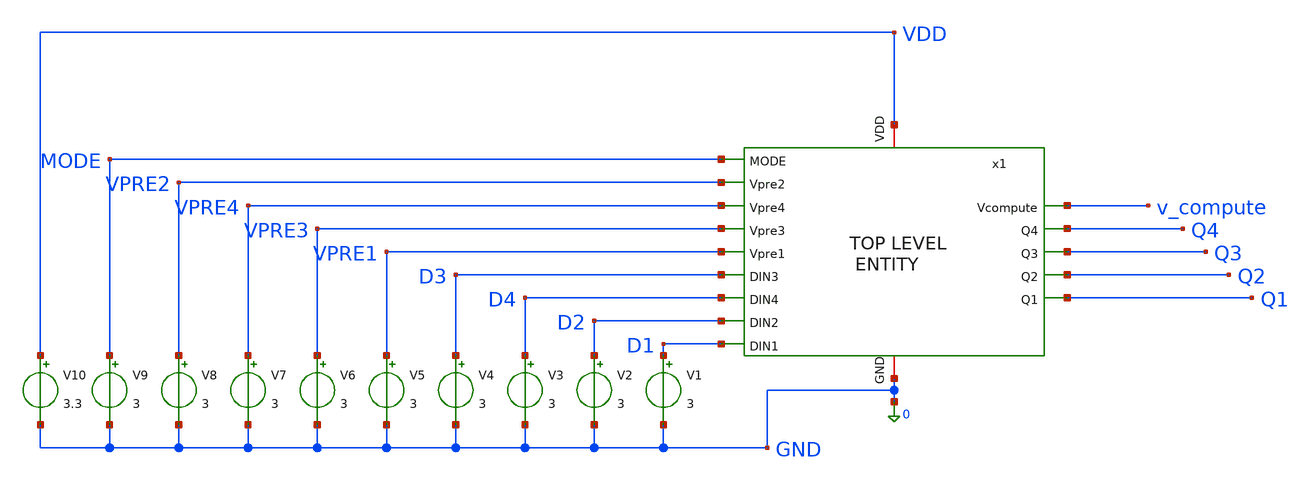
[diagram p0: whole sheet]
** sch_path: src/schematic/INTEGRASI/integrasi_TB.sch
**.subckt integrasi_TB
x1 VDD MODE 0 VPRE2 VPRE4 VPRE3 VPRE1 D3 D4 v_compute Q4 Q3 Q2 Q1 D2 D1 integrasi
V1 D1 0 3
V2 D2 0 3
V3 D4 0 3
V4 D3 0 3
V5 VPRE1 0 3
V6 VPRE3 0 3
V7 VPRE4 0 3
V8 VPRE2 0 3
V9 MODE 0 3
V10 VDD 0 3.3
**.ends

* expanding   symbol:  src/schematic/INTEGRASI/integrasi.sym # of pins=16
** sym_path: src/schematic/INTEGRASI/integrasi.sym
** sch_path: src/schematic/INTEGRASI/integrasi.sch
.subckt integrasi VDD MODE GND Vpre2 Vpre4 Vpre3 Vpre1 DIN3 DIN4 Vcompute Q4 Q3 Q2 Q1 DIN2 DIN1
*.ipin Vpre1
*.ipin Vpre2
*.ipin Vpre3
*.ipin Vpre4
*.ipin DIN4
*.ipin DIN3
*.ipin DIN2
*.ipin DIN1
*.ipin MODE
*.iopin VDD
*.iopin GND
*.opin Vcompute
*.opin Q4
*.opin Q3
*.opin Q2
*.opin Q1
x1 net1 net2 net4 net3 net19 net20 net21 net18 net5 net7 net27 net26 net28 net29 Q4 Q3 Q2 Q1 net8
+ net12 Vcompute memori
x2 net5 net2 Vpre2 net6 MODE transgate
x3 net5 net3 Vpre3 net6 MODE transgate
x4 net5 net4 Vpre4 net6 MODE transgate
x5 net5 net1 Vpre1 net6 MODE transgate
x6 VDD net7 net11 net8 net10 transgate
x7 VDD net7 VDD net8 net9 transgate
x8 VDD net10 net9 net8 inverter
x9 VDD net11 net8 net13 net14 net15 net16 dac
x10 net5 net1 net12 net2 net3 net4 net8 en_compute
x11 VDD net15 DIN2 net8 MODE transgate
x12 VDD net14 DIN4 net8 MODE transgate
x13 VDD net13 DIN3 net8 MODE transgate
x14 VDD net16 DIN1 net8 MODE transgate
x15 VDD net20 DIN2 GND net17 transgate
x16 VDD net19 DIN4 GND net17 transgate
x17 VDD net18 DIN3 GND net17 transgate
x18 VDD net21 DIN1 GND net17 transgate
x19 VDD net23 net20 GND net17 transgate
x20 VDD net24 net19 GND net17 transgate
x21 VDD net25 net18 GND net17 transgate
x22 VDD net22 net21 GND net17 transgate
x23 VDD net25 net29 GND inverter
x24 VDD net24 net28 GND inverter
x25 VDD net23 net26 GND inverter
x26 VDD net22 net27 GND inverter
x27 VDD MODE net17 GND inverter
.ends


* expanding   symbol:  memori.sym # of pins=21
** sym_path: src/schematic/MEMORY/memori.sym
** sch_path: src/schematic/MEMORY/memori.sch
.subckt memori Vpre1 Vpre2 Vpre4 Vpre3 BL4 BL2 BL1 BL3 VDD WL BLB1 BLB2 BLB4 BLB3 Q4 Q3 Q2 Q1 GND
+ en_comp Vout
*.iopin GND
*.iopin VDD
*.iopin WL
*.iopin Q1
*.iopin Q2
*.iopin Q3
*.iopin Q4
*.iopin Vpre4
*.iopin Vpre3
*.iopin Vpre2
*.iopin Vpre1
*.iopin en_comp
*.iopin Vout
*.iopin BLB1
*.iopin BLB2
*.iopin BLB3
*.iopin BLB4
*.iopin BL1
*.iopin BL2
*.iopin BL3
*.iopin BL4
x1 net1 net2 net3 net4 net5 net6 6T4bit
x2 net7 net8 net9 net10 net11 GND 6T4bit
x3 net12 net13 net14 net15 net16 GND 6T4bit
x4 net17 net18 net19 net20 net21 net22 6T4bit
XM1 GND en_comp BLB4 VDD pfet_03v3 L=0.28u W=0.22u nf=1 ad='int((nf+1)/2) * W/nf * 0.18u' as='int((nf+2)/2) * W/nf * 0.18u'
+ pd='2*int((nf+1)/2) * (W/nf + 0.18u)' ps='2*int((nf+2)/2) * (W/nf + 0.18u)' nrd='0.18u / W' nrs='0.18u / W'
+ sa=0 sb=0 sd=0 m=1
XM2 GND en_comp BLB3 VDD pfet_03v3 L=0.28u W=0.22u nf=1 ad='int((nf+1)/2) * W/nf * 0.18u' as='int((nf+2)/2) * W/nf * 0.18u'
+ pd='2*int((nf+1)/2) * (W/nf + 0.18u)' ps='2*int((nf+2)/2) * (W/nf + 0.18u)' nrd='0.18u / W' nrs='0.18u / W'
+ sa=0 sb=0 sd=0 m=1
XM3 GND en_comp BLB2 VDD pfet_03v3 L=0.28u W=0.22u nf=1 ad='int((nf+1)/2) * W/nf * 0.18u' as='int((nf+2)/2) * W/nf * 0.18u'
+ pd='2*int((nf+1)/2) * (W/nf + 0.18u)' ps='2*int((nf+2)/2) * (W/nf + 0.18u)' nrd='0.18u / W' nrs='0.18u / W'
+ sa=0 sb=0 sd=0 m=1
XM4 GND en_comp BLB1 VDD pfet_03v3 L=0.28u W=0.22u nf=1 ad='int((nf+1)/2) * W/nf * 0.18u' as='int((nf+2)/2) * W/nf * 0.18u'
+ pd='2*int((nf+1)/2) * (W/nf + 0.18u)' ps='2*int((nf+2)/2) * (W/nf + 0.18u)' nrd='0.18u / W' nrs='0.18u / W'
+ sa=0 sb=0 sd=0 m=1
XM5 BLB4 en_comp GND GND nfet_03v3 L=0.28u W=0.22u nf=1 ad='int((nf+1)/2) * W/nf * 0.18u' as='int((nf+2)/2) * W/nf * 0.18u'
+ pd='2*int((nf+1)/2) * (W/nf + 0.18u)' ps='2*int((nf+2)/2) * (W/nf + 0.18u)' nrd='0.18u / W' nrs='0.18u / W'
+ sa=0 sb=0 sd=0 m=1
XM6 BLB3 en_comp GND GND nfet_03v3 L=0.28u W=0.22u nf=1 ad='int((nf+1)/2) * W/nf * 0.18u' as='int((nf+2)/2) * W/nf * 0.18u'
+ pd='2*int((nf+1)/2) * (W/nf + 0.18u)' ps='2*int((nf+2)/2) * (W/nf + 0.18u)' nrd='0.18u / W' nrs='0.18u / W'
+ sa=0 sb=0 sd=0 m=1
XM7 BLB2 en_comp GND GND nfet_03v3 L=0.28u W=0.22u nf=1 ad='int((nf+1)/2) * W/nf * 0.18u' as='int((nf+2)/2) * W/nf * 0.18u'
+ pd='2*int((nf+1)/2) * (W/nf + 0.18u)' ps='2*int((nf+2)/2) * (W/nf + 0.18u)' nrd='0.18u / W' nrs='0.18u / W'
+ sa=0 sb=0 sd=0 m=1
XM8 BLB1 en_comp GND GND nfet_03v3 L=0.28u W=0.22u nf=1 ad='int((nf+1)/2) * W/nf * 0.18u' as='int((nf+2)/2) * W/nf * 0.18u'
+ pd='2*int((nf+1)/2) * (W/nf + 0.18u)' ps='2*int((nf+2)/2) * (W/nf + 0.18u)' nrd='0.18u / W' nrs='0.18u / W'
+ sa=0 sb=0 sd=0 m=1
XM9 BLB4 Vpre4 VDD VDD pfet_03v3 L=0.28u W=0.22u nf=1 ad='int((nf+1)/2) * W/nf * 0.18u' as='int((nf+2)/2) * W/nf * 0.18u'
+ pd='2*int((nf+1)/2) * (W/nf + 0.18u)' ps='2*int((nf+2)/2) * (W/nf + 0.18u)' nrd='0.18u / W' nrs='0.18u / W'
+ sa=0 sb=0 sd=0 m=1
XM10 BLB3 Vpre3 VDD VDD pfet_03v3 L=0.28u W=0.22u nf=1 ad='int((nf+1)/2) * W/nf * 0.18u' as='int((nf+2)/2) * W/nf * 0.18u'
+ pd='2*int((nf+1)/2) * (W/nf + 0.18u)' ps='2*int((nf+2)/2) * (W/nf + 0.18u)' nrd='0.18u / W' nrs='0.18u / W'
+ sa=0 sb=0 sd=0 m=1
XM11 BLB2 Vpre2 VDD VDD pfet_03v3 L=0.28u W=0.22u nf=1 ad='int((nf+1)/2) * W/nf * 0.18u' as='int((nf+2)/2) * W/nf * 0.18u'
+ pd='2*int((nf+1)/2) * (W/nf + 0.18u)' ps='2*int((nf+2)/2) * (W/nf + 0.18u)' nrd='0.18u / W' nrs='0.18u / W'
+ sa=0 sb=0 sd=0 m=1
XM12 BLB1 Vpre1 VDD VDD pfet_03v3 L=0.28u W=0.22u nf=1 ad='int((nf+1)/2) * W/nf * 0.18u' as='int((nf+2)/2) * W/nf * 0.18u'
+ pd='2*int((nf+1)/2) * (W/nf + 0.18u)' ps='2*int((nf+2)/2) * (W/nf + 0.18u)' nrd='0.18u / W' nrs='0.18u / W'
+ sa=0 sb=0 sd=0 m=1
XM13 BL1 Vpre1 VDD VDD pfet_03v3 L=0.28u W=0.22u nf=1 ad='int((nf+1)/2) * W/nf * 0.18u' as='int((nf+2)/2) * W/nf * 0.18u'
+ pd='2*int((nf+1)/2) * (W/nf + 0.18u)' ps='2*int((nf+2)/2) * (W/nf + 0.18u)' nrd='0.18u / W' nrs='0.18u / W'
+ sa=0 sb=0 sd=0 m=1
XM14 BL2 Vpre2 VDD VDD pfet_03v3 L=0.28u W=0.22u nf=1 ad='int((nf+1)/2) * W/nf * 0.18u' as='int((nf+2)/2) * W/nf * 0.18u'
+ pd='2*int((nf+1)/2) * (W/nf + 0.18u)' ps='2*int((nf+2)/2) * (W/nf + 0.18u)' nrd='0.18u / W' nrs='0.18u / W'
+ sa=0 sb=0 sd=0 m=1
XM15 BL3 Vpre3 VDD VDD pfet_03v3 L=0.28u W=0.22u nf=1 ad='int((nf+1)/2) * W/nf * 0.18u' as='int((nf+2)/2) * W/nf * 0.18u'
+ pd='2*int((nf+1)/2) * (W/nf + 0.18u)' ps='2*int((nf+2)/2) * (W/nf + 0.18u)' nrd='0.18u / W' nrs='0.18u / W'
+ sa=0 sb=0 sd=0 m=1
XM16 BL4 Vpre4 VDD VDD pfet_03v3 L=0.28u W=0.22u nf=1 ad='int((nf+1)/2) * W/nf * 0.18u' as='int((nf+2)/2) * W/nf * 0.18u'
+ pd='2*int((nf+1)/2) * (W/nf + 0.18u)' ps='2*int((nf+2)/2) * (W/nf + 0.18u)' nrd='0.18u / W' nrs='0.18u / W'
+ sa=0 sb=0 sd=0 m=1
XM17 BLB4 Vpre4 BL4 net23 pfet_03v3 L=0.28u W=0.22u nf=1 ad='int((nf+1)/2) * W/nf * 0.18u' as='int((nf+2)/2) * W/nf * 0.18u'
+ pd='2*int((nf+1)/2) * (W/nf + 0.18u)' ps='2*int((nf+2)/2) * (W/nf + 0.18u)' nrd='0.18u / W' nrs='0.18u / W'
+ sa=0 sb=0 sd=0 m=1
XM18 BLB3 Vpre3 BL3 net24 pfet_03v3 L=0.28u W=0.22u nf=1 ad='int((nf+1)/2) * W/nf * 0.18u' as='int((nf+2)/2) * W/nf * 0.18u'
+ pd='2*int((nf+1)/2) * (W/nf + 0.18u)' ps='2*int((nf+2)/2) * (W/nf + 0.18u)' nrd='0.18u / W' nrs='0.18u / W'
+ sa=0 sb=0 sd=0 m=1
XM19 BLB2 Vpre2 BL2 net25 pfet_03v3 L=0.28u W=0.22u nf=1 ad='int((nf+1)/2) * W/nf * 0.18u' as='int((nf+2)/2) * W/nf * 0.18u'
+ pd='2*int((nf+1)/2) * (W/nf + 0.18u)' ps='2*int((nf+2)/2) * (W/nf + 0.18u)' nrd='0.18u / W' nrs='0.18u / W'
+ sa=0 sb=0 sd=0 m=1
XM20 BLB1 Vpre1 BL1 net26 pfet_03v3 L=0.28u W=0.22u nf=1 ad='int((nf+1)/2) * W/nf * 0.18u' as='int((nf+2)/2) * W/nf * 0.18u'
+ pd='2*int((nf+1)/2) * (W/nf + 0.18u)' ps='2*int((nf+2)/2) * (W/nf + 0.18u)' nrd='0.18u / W' nrs='0.18u / W'
+ sa=0 sb=0 sd=0 m=1
.ends


* expanding   symbol:  transgate.sym # of pins=5
** sym_path: src/schematic/INTEGRASI/transgate.sym
** sch_path: src/schematic/INTEGRASI/transgate.sch
.subckt transgate vdd s d gnd c
*.iopin gnd
*.iopin vdd
*.iopin c
*.ipin d
*.opin s
XM1 d c s gnd nfet_03v3 L=0.28u W=0.22u nf=1 ad='int((nf+1)/2) * W/nf * 0.18u' as='int((nf+2)/2) * W/nf * 0.18u'
+ pd='2*int((nf+1)/2) * (W/nf + 0.18u)' ps='2*int((nf+2)/2) * (W/nf + 0.18u)' nrd='0.18u / W' nrs='0.18u / W'
+ sa=0 sb=0 sd=0 m=1
XM2 d net1 s vdd pfet_03v3 L=0.28u W=0.22u nf=1 ad='int((nf+1)/2) * W/nf * 0.18u' as='int((nf+2)/2) * W/nf * 0.18u'
+ pd='2*int((nf+1)/2) * (W/nf + 0.18u)' ps='2*int((nf+2)/2) * (W/nf + 0.18u)' nrd='0.18u / W' nrs='0.18u / W'
+ sa=0 sb=0 sd=0 m=1
x1 vdd c net1 gnd inverter
.ends


* expanding   symbol:  inverter.sym # of pins=4
** sym_path: src/schematic/INTEGRASI/inverter.sym
** sch_path: src/schematic/INTEGRASI/inverter.sch
.subckt inverter vdd vi vo gnd
*.ipin vi
*.opin vo
*.iopin vdd
*.iopin gnd
XM1 vo vi vdd vdd pfet_03v3 L=0.28u W=0.22u nf=1 ad='int((nf+1)/2) * W/nf * 0.18u' as='int((nf+2)/2) * W/nf * 0.18u'
+ pd='2*int((nf+1)/2) * (W/nf + 0.18u)' ps='2*int((nf+2)/2) * (W/nf + 0.18u)' nrd='0.18u / W' nrs='0.18u / W'
+ sa=0 sb=0 sd=0 m=1
XM2 vo vi gnd gnd nfet_03v3 L=0.28u W=0.22u nf=1 ad='int((nf+1)/2) * W/nf * 0.18u' as='int((nf+2)/2) * W/nf * 0.18u'
+ pd='2*int((nf+1)/2) * (W/nf + 0.18u)' ps='2*int((nf+2)/2) * (W/nf + 0.18u)' nrd='0.18u / W' nrs='0.18u / W'
+ sa=0 sb=0 sd=0 m=1
.ends


* expanding   symbol:  dac.sym # of pins=7
** sym_path: src/schematic/INTEGRASI/dac.sym
** sch_path: src/schematic/INTEGRASI/dac.sch
.subckt dac VDD Vout GND V3 V4 V2 V1
*.ipin V1
*.ipin V2
*.ipin V3
*.ipin V4
*.opin Vout
*.iopin VDD
*.iopin GND
R1 VDD Vout 1k m=1
R2 VDD net3 1k m=1
XQ1 net1 net3 V4 V4 nfet_03v3 L=0.28u W=1u nf=1 ad='int((nf+1)/2) * W/nf * 0.18u' as='int((nf+2)/2) * W/nf * 0.18u'
+ pd='2*int((nf+1)/2) * (W/nf + 0.18u)' ps='2*int((nf+2)/2) * (W/nf + 0.18u)' nrd='0.18u / W' nrs='0.18u / W'
+ sa=0 sb=0 sd=0 m=1
XQ2 net4 net3 V4 V4 nfet_03v3 L=0.28u W=2u nf=1 ad='int((nf+1)/2) * W/nf * 0.18u' as='int((nf+2)/2) * W/nf * 0.18u'
+ pd='2*int((nf+1)/2) * (W/nf + 0.18u)' ps='2*int((nf+2)/2) * (W/nf + 0.18u)' nrd='0.18u / W' nrs='0.18u / W'
+ sa=0 sb=0 sd=0 m=1
XQ3 net5 net3 V4 V4 nfet_03v3 L=0.28u W=4u nf=1 ad='int((nf+1)/2) * W/nf * 0.18u' as='int((nf+2)/2) * W/nf * 0.18u'
+ pd='2*int((nf+1)/2) * (W/nf + 0.18u)' ps='2*int((nf+2)/2) * (W/nf + 0.18u)' nrd='0.18u / W' nrs='0.18u / W'
+ sa=0 sb=0 sd=0 m=1
XQ4 net2 net3 V4 V4 nfet_03v3 L=0.28u W=8u nf=1 ad='int((nf+1)/2) * W/nf * 0.18u' as='int((nf+2)/2) * W/nf * 0.18u'
+ pd='2*int((nf+1)/2) * (W/nf + 0.18u)' ps='2*int((nf+2)/2) * (W/nf + 0.18u)' nrd='0.18u / W' nrs='0.18u / W'
+ sa=0 sb=0 sd=0 m=1
XQ0 V4 net3 net3 V4 nfet_03v3 L=0.28u W=1u nf=1 ad='int((nf+1)/2) * W/nf * 0.18u' as='int((nf+2)/2) * W/nf * 0.18u'
+ pd='2*int((nf+1)/2) * (W/nf + 0.18u)' ps='2*int((nf+2)/2) * (W/nf + 0.18u)' nrd='0.18u / W' nrs='0.18u / W'
+ sa=0 sb=0 sd=0 m=1
XTGN1 Vout V1 net1 V4 nfet_03v3 L=0.28u W=5u nf=1 ad='int((nf+1)/2) * W/nf * 0.18u' as='int((nf+2)/2) * W/nf * 0.18u'
+ pd='2*int((nf+1)/2) * (W/nf + 0.18u)' ps='2*int((nf+2)/2) * (W/nf + 0.18u)' nrd='0.18u / W' nrs='0.18u / W'
+ sa=0 sb=0 sd=0 m=1
XTGN2 Vout V2 net4 V4 nfet_03v3 L=0.28u W=5u nf=1 ad='int((nf+1)/2) * W/nf * 0.18u' as='int((nf+2)/2) * W/nf * 0.18u'
+ pd='2*int((nf+1)/2) * (W/nf + 0.18u)' ps='2*int((nf+2)/2) * (W/nf + 0.18u)' nrd='0.18u / W' nrs='0.18u / W'
+ sa=0 sb=0 sd=0 m=1
XTGN3 Vout V3 net5 V4 nfet_03v3 L=0.28u W=5u nf=1 ad='int((nf+1)/2) * W/nf * 0.18u' as='int((nf+2)/2) * W/nf * 0.18u'
+ pd='2*int((nf+1)/2) * (W/nf + 0.18u)' ps='2*int((nf+2)/2) * (W/nf + 0.18u)' nrd='0.18u / W' nrs='0.18u / W'
+ sa=0 sb=0 sd=0 m=1
XTGN4 Vout V4 net2 V4 nfet_03v3 L=0.28u W=5u nf=1 ad='int((nf+1)/2) * W/nf * 0.18u' as='int((nf+2)/2) * W/nf * 0.18u'
+ pd='2*int((nf+1)/2) * (W/nf + 0.18u)' ps='2*int((nf+2)/2) * (W/nf + 0.18u)' nrd='0.18u / W' nrs='0.18u / W'
+ sa=0 sb=0 sd=0 m=1
XTGP1 net1 VB1 Vout VDD pfet_03v3 L=0.28u W=10u nf=1 ad='int((nf+1)/2) * W/nf * 0.18u' as='int((nf+2)/2) * W/nf * 0.18u'
+ pd='2*int((nf+1)/2) * (W/nf + 0.18u)' ps='2*int((nf+2)/2) * (W/nf + 0.18u)' nrd='0.18u / W' nrs='0.18u / W'
+ sa=0 sb=0 sd=0 m=1
XIN1 VB1 V1 V4 V4 nfet_03v3 L=0.28u W=1u nf=1 ad='int((nf+1)/2) * W/nf * 0.18u' as='int((nf+2)/2) * W/nf * 0.18u'
+ pd='2*int((nf+1)/2) * (W/nf + 0.18u)' ps='2*int((nf+2)/2) * (W/nf + 0.18u)' nrd='0.18u / W' nrs='0.18u / W'
+ sa=0 sb=0 sd=0 m=1
XIP1 VB1 V1 VDD VDD pfet_03v3 L=0.28u W=2u nf=1 ad='int((nf+1)/2) * W/nf * 0.18u' as='int((nf+2)/2) * W/nf * 0.18u'
+ pd='2*int((nf+1)/2) * (W/nf + 0.18u)' ps='2*int((nf+2)/2) * (W/nf + 0.18u)' nrd='0.18u / W' nrs='0.18u / W'
+ sa=0 sb=0 sd=0 m=1
XIN2 VB2 V2 V4 V4 nfet_03v3 L=0.28u W=1u nf=1 ad='int((nf+1)/2) * W/nf * 0.18u' as='int((nf+2)/2) * W/nf * 0.18u'
+ pd='2*int((nf+1)/2) * (W/nf + 0.18u)' ps='2*int((nf+2)/2) * (W/nf + 0.18u)' nrd='0.18u / W' nrs='0.18u / W'
+ sa=0 sb=0 sd=0 m=1
XIP2 VB2 V2 VDD VDD pfet_03v3 L=0.28u W=2u nf=1 ad='int((nf+1)/2) * W/nf * 0.18u' as='int((nf+2)/2) * W/nf * 0.18u'
+ pd='2*int((nf+1)/2) * (W/nf + 0.18u)' ps='2*int((nf+2)/2) * (W/nf + 0.18u)' nrd='0.18u / W' nrs='0.18u / W'
+ sa=0 sb=0 sd=0 m=1
XIN3 VB3 V3 V4 V4 nfet_03v3 L=0.28u W=1u nf=1 ad='int((nf+1)/2) * W/nf * 0.18u' as='int((nf+2)/2) * W/nf * 0.18u'
+ pd='2*int((nf+1)/2) * (W/nf + 0.18u)' ps='2*int((nf+2)/2) * (W/nf + 0.18u)' nrd='0.18u / W' nrs='0.18u / W'
+ sa=0 sb=0 sd=0 m=1
XIP3 VB3 V3 VDD VDD pfet_03v3 L=0.28u W=2u nf=1 ad='int((nf+1)/2) * W/nf * 0.18u' as='int((nf+2)/2) * W/nf * 0.18u'
+ pd='2*int((nf+1)/2) * (W/nf + 0.18u)' ps='2*int((nf+2)/2) * (W/nf + 0.18u)' nrd='0.18u / W' nrs='0.18u / W'
+ sa=0 sb=0 sd=0 m=1
XIN4 VB4 V4 V4 V4 nfet_03v3 L=0.28u W=1u nf=1 ad='int((nf+1)/2) * W/nf * 0.18u' as='int((nf+2)/2) * W/nf * 0.18u'
+ pd='2*int((nf+1)/2) * (W/nf + 0.18u)' ps='2*int((nf+2)/2) * (W/nf + 0.18u)' nrd='0.18u / W' nrs='0.18u / W'
+ sa=0 sb=0 sd=0 m=1
XIP4 VB4 V4 VDD VDD pfet_03v3 L=0.28u W=2u nf=1 ad='int((nf+1)/2) * W/nf * 0.18u' as='int((nf+2)/2) * W/nf * 0.18u'
+ pd='2*int((nf+1)/2) * (W/nf + 0.18u)' ps='2*int((nf+2)/2) * (W/nf + 0.18u)' nrd='0.18u / W' nrs='0.18u / W'
+ sa=0 sb=0 sd=0 m=1
XTGP2 net4 VB2 Vout VDD pfet_03v3 L=0.28u W=10u nf=1 ad='int((nf+1)/2) * W/nf * 0.18u' as='int((nf+2)/2) * W/nf * 0.18u'
+ pd='2*int((nf+1)/2) * (W/nf + 0.18u)' ps='2*int((nf+2)/2) * (W/nf + 0.18u)' nrd='0.18u / W' nrs='0.18u / W'
+ sa=0 sb=0 sd=0 m=1
XTGP3 net5 VB3 Vout VDD pfet_03v3 L=0.28u W=10u nf=1 ad='int((nf+1)/2) * W/nf * 0.18u' as='int((nf+2)/2) * W/nf * 0.18u'
+ pd='2*int((nf+1)/2) * (W/nf + 0.18u)' ps='2*int((nf+2)/2) * (W/nf + 0.18u)' nrd='0.18u / W' nrs='0.18u / W'
+ sa=0 sb=0 sd=0 m=1
XTGP4 net2 VB4 Vout VDD pfet_03v3 L=0.28u W=10u nf=1 ad='int((nf+1)/2) * W/nf * 0.18u' as='int((nf+2)/2) * W/nf * 0.18u'
+ pd='2*int((nf+1)/2) * (W/nf + 0.18u)' ps='2*int((nf+2)/2) * (W/nf + 0.18u)' nrd='0.18u / W' nrs='0.18u / W'
+ sa=0 sb=0 sd=0 m=1
.ends


* expanding   symbol:  en_compute.sym # of pins=7
** sym_path: src/schematic/EN-COMPUTE/en_compute.sym
** sch_path: src/schematic/EN-COMPUTE/en_compute.sch
.subckt en_compute VDD A en_cmpt B C D GND
*.iopin VDD
*.iopin GND
*.iopin en_cmpt
*.iopin D
*.iopin C
*.iopin B
*.iopin A
x1 VDD A B net1 GND norGate
x3 VDD net1 C net2 GND norGate
x5 VDD net2 D en_cmpt GND norGate
.ends


* expanding   symbol:  src/schematic/6T4BIT/6T4bit.sch # of pins=6
** sym_path: src/schematic/6T4BIT/6T4bit.sch
** sch_path: src/schematic/6T4BIT/6T4bit.sch
.subckt 6T4bit VDD WL BLB BL Q GND
*.iopin BLB
*.iopin GND
*.iopin Q
*.iopin VDD
*.iopin BL
*.iopin WL
XSR1_M6 Q WL BL GND nfet_03v3 L=0.28u W=0.22u nf=1 ad='int((nf+1)/2) * W/nf * 0.18u' as='int((nf+2)/2) * W/nf * 0.18u'
+ pd='2*int((nf+1)/2) * (W/nf + 0.18u)' ps='2*int((nf+2)/2) * (W/nf + 0.18u)' nrd='0.18u / W' nrs='0.18u / W'
+ sa=0 sb=0 sd=0 m=1
XSR1_M3 VDD net1 Q VDD pfet_03v3 L=0.28u W=0.22u nf=1 ad='int((nf+1)/2) * W/nf * 0.18u' as='int((nf+2)/2) * W/nf * 0.18u'
+ pd='2*int((nf+1)/2) * (W/nf + 0.18u)' ps='2*int((nf+2)/2) * (W/nf + 0.18u)' nrd='0.18u / W' nrs='0.18u / W'
+ sa=0 sb=0 sd=0 m=1
XSR1_M4 net1 net2 VDD VDD pfet_03v3 L=0.28u W=0.22u nf=1 ad='int((nf+1)/2) * W/nf * 0.18u' as='int((nf+2)/2) * W/nf * 0.18u'
+ pd='2*int((nf+1)/2) * (W/nf + 0.18u)' ps='2*int((nf+2)/2) * (W/nf + 0.18u)' nrd='0.18u / W' nrs='0.18u / W'
+ sa=0 sb=0 sd=0 m=1
XSR1_M5 BLB WL net1 GND nfet_03v3 L=0.28u W=0.22u nf=1 ad='int((nf+1)/2) * W/nf * 0.18u' as='int((nf+2)/2) * W/nf * 0.18u'
+ pd='2*int((nf+1)/2) * (W/nf + 0.18u)' ps='2*int((nf+2)/2) * (W/nf + 0.18u)' nrd='0.18u / W' nrs='0.18u / W'
+ sa=0 sb=0 sd=0 m=1
XSR1_M1 GND net1 Q GND nfet_03v3 L=0.28u W=0.22u nf=1 ad='int((nf+1)/2) * W/nf * 0.18u' as='int((nf+2)/2) * W/nf * 0.18u'
+ pd='2*int((nf+1)/2) * (W/nf + 0.18u)' ps='2*int((nf+2)/2) * (W/nf + 0.18u)' nrd='0.18u / W' nrs='0.18u / W'
+ sa=0 sb=0 sd=0 m=1
XSR1_M2 net1 net2 GND GND nfet_03v3 L=0.28u W=0.22u nf=1 ad='int((nf+1)/2) * W/nf * 0.18u' as='int((nf+2)/2) * W/nf * 0.18u'
+ pd='2*int((nf+1)/2) * (W/nf + 0.18u)' ps='2*int((nf+2)/2) * (W/nf + 0.18u)' nrd='0.18u / W' nrs='0.18u / W'
+ sa=0 sb=0 sd=0 m=1
.ends


* expanding   symbol:  src/schematic/NOR/norGate.sym # of pins=5
** sym_path: src/schematic/INTEGRASI/norGate.sym
** sch_path: src/schematic/INTEGRASI/norGate.sch
.subckt norGate vdd a b y gnd
*.iopin gnd
*.iopin vdd
*.ipin a
*.ipin b
*.opin y
XM1 y a net1 vdd pfet_03v3 L=0.28u W=0.22u nf=1 ad='int((nf+1)/2) * W/nf * 0.18u' as='int((nf+2)/2) * W/nf * 0.18u'
+ pd='2*int((nf+1)/2) * (W/nf + 0.18u)' ps='2*int((nf+2)/2) * (W/nf + 0.18u)' nrd='0.18u / W' nrs='0.18u / W'
+ sa=0 sb=0 sd=0 m=1
XM2 net1 a vdd vdd pfet_03v3 L=0.28u W=0.22u nf=1 ad='int((nf+1)/2) * W/nf * 0.18u' as='int((nf+2)/2) * W/nf * 0.18u'
+ pd='2*int((nf+1)/2) * (W/nf + 0.18u)' ps='2*int((nf+2)/2) * (W/nf + 0.18u)' nrd='0.18u / W' nrs='0.18u / W'
+ sa=0 sb=0 sd=0 m=1
XM3 y a gnd gnd nfet_03v3 L=0.28u W=0.22u nf=1 ad='int((nf+1)/2) * W/nf * 0.18u' as='int((nf+2)/2) * W/nf * 0.18u'
+ pd='2*int((nf+1)/2) * (W/nf + 0.18u)' ps='2*int((nf+2)/2) * (W/nf + 0.18u)' nrd='0.18u / W' nrs='0.18u / W'
+ sa=0 sb=0 sd=0 m=1
XM4 y a gnd gnd nfet_03v3 L=0.28u W=0.22u nf=1 ad='int((nf+1)/2) * W/nf * 0.18u' as='int((nf+2)/2) * W/nf * 0.18u'
+ pd='2*int((nf+1)/2) * (W/nf + 0.18u)' ps='2*int((nf+2)/2) * (W/nf + 0.18u)' nrd='0.18u / W' nrs='0.18u / W'
+ sa=0 sb=0 sd=0 m=1
.ends

.end
